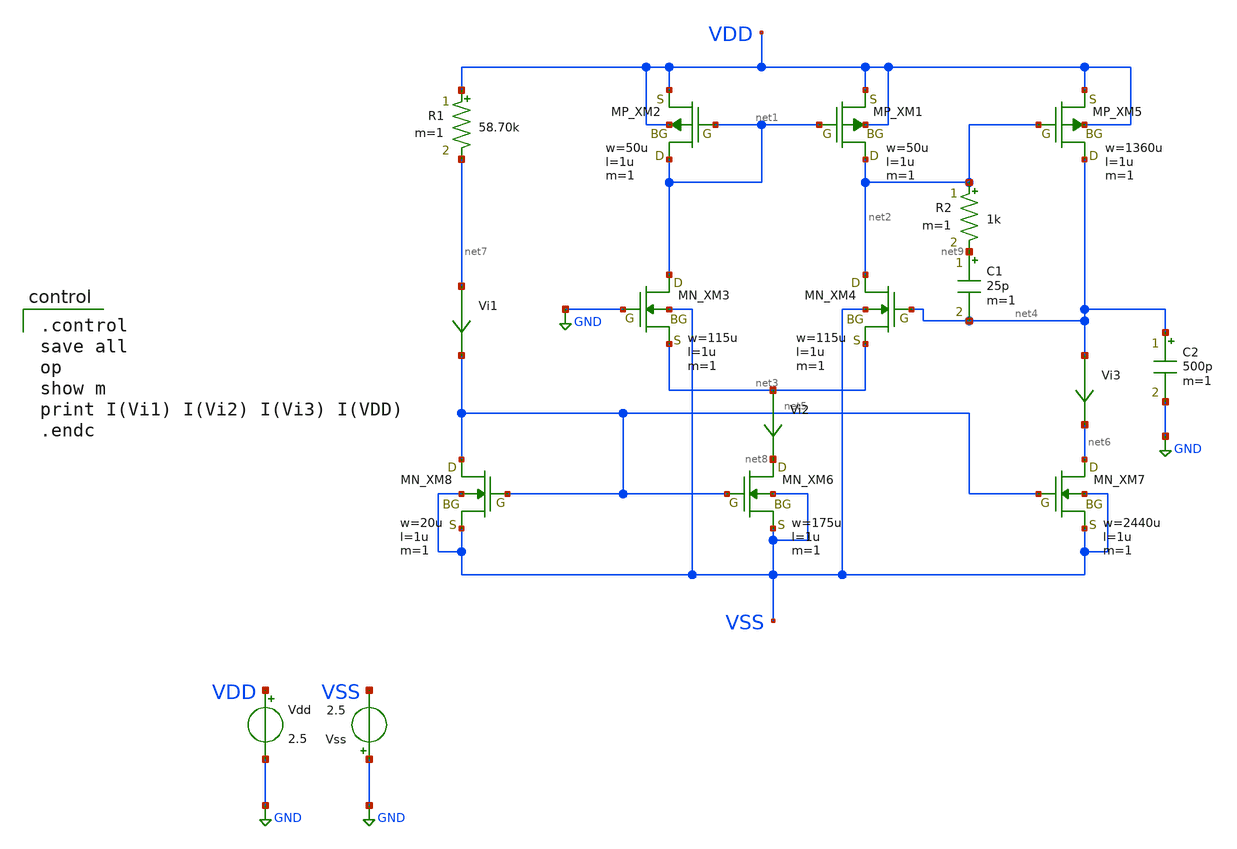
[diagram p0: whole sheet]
** sch_path: OPAF2026/cascode.sch
**.subckt cascode
XXM1 net2 net1 VDD VDD PMOS w=50u l=1u nrd=0 nrs=0 m=1
XXM2 net1 net1 VDD VDD PMOS w=50u l=1u nrd=0 nrs=0 m=1
XXM3 net1 GND net3 VSS NMOS w=115u l=1u nrd=0 nrs=0 m=1
XXM4 net2 net4 net3 VSS NMOS w=115u l=1u nrd=0 nrs=0 m=1
XXM5 net4 net2 VDD VDD PMOS w=1360u l=1u nrd=0 nrs=0 m=1
XXM6 net8 net5 VSS VSS NMOS w=175u l=1u nrd=0 nrs=0 m=1
XXM7 net6 net5 VSS VSS NMOS w=2440u l=1u nrd=0 nrs=0 m=1
XXM8 net5 net5 VSS VSS NMOS w=20u l=1u nrd=0 nrs=0 m=1
Vdd VDD GND 2.5
Vss GND VSS 2.5
C2 net4 GND 500p m=1
Vi1 net7 net5 0
.save i(vi1)
Vi2 net3 net8 0
.save i(vi2)
Vi3 net4 net6 0
.save i(vi3)
R1 VDD net7 58.70k m=1
R2 net2 net9 1k m=1
C1 net9 net4 25p m=1
**** begin user architecture code

.control
save all
op
show m
print I(Vi1) I(Vi2) I(Vi3) I(VDD)
.endc

 .include $::LIB/ip62_models
**** end user architecture code
**.ends
.GLOBAL GND
.end
